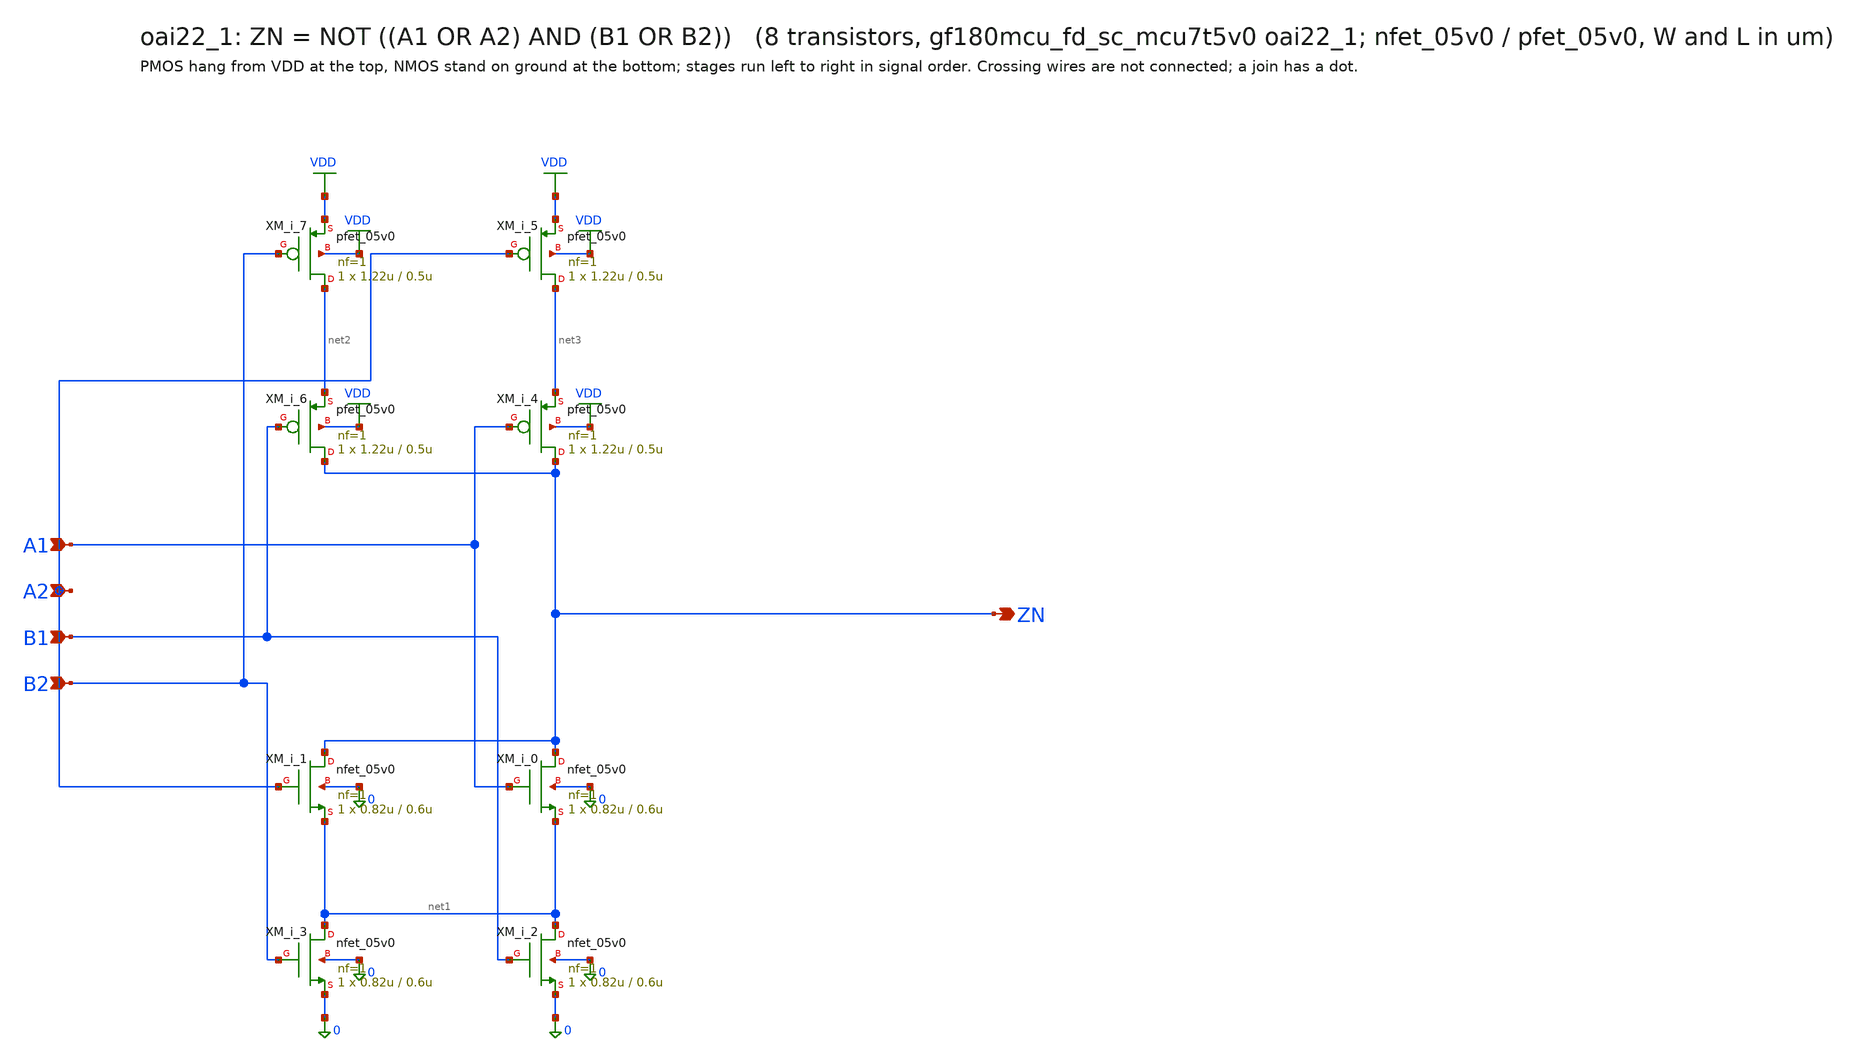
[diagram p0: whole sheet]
** sch_path: xschem/cells_tx/oai22_1.sch
**.subckt oai22_1 A1 A2 B1 B2 ZN
*.ipin A1
*.ipin A2
*.ipin B1
*.ipin B2
*.opin ZN
XM_i_3 net1 B2 0 0 nfet_05v0 L=0.6u W=0.82u nf=1 ad=4.1e-13 as=4.1e-13 pd=2.64e-06 ps=2.64e-06 nrd=0
+ nrs=0 sa=0 sb=0 sd=0 m=1
XM_i_2 net1 B1 0 0 nfet_05v0 L=0.6u W=0.82u nf=1 ad=4.1e-13 as=4.1e-13 pd=2.64e-06 ps=2.64e-06 nrd=0
+ nrs=0 sa=0 sb=0 sd=0 m=1
XM_i_0 ZN A1 net1 0 nfet_05v0 L=0.6u W=0.82u nf=1 ad=4.1e-13 as=4.1e-13 pd=2.64e-06 ps=2.64e-06
+ nrd=0 nrs=0 sa=0 sb=0 sd=0 m=1
XM_i_1 ZN A2 net1 0 nfet_05v0 L=0.6u W=0.82u nf=1 ad=4.1e-13 as=4.1e-13 pd=2.64e-06 ps=2.64e-06
+ nrd=0 nrs=0 sa=0 sb=0 sd=0 m=1
XM_i_7 net2 B2 VDD VDD pfet_05v0 L=0.5u W=1.22u nf=1 ad=6.1e-13 as=6.1e-13 pd=3.44e-06 ps=3.44e-06
+ nrd=0 nrs=0 sa=0 sb=0 sd=0 m=1
XM_i_6 ZN B1 net2 VDD pfet_05v0 L=0.5u W=1.22u nf=1 ad=6.1e-13 as=6.1e-13 pd=3.44e-06 ps=3.44e-06
+ nrd=0 nrs=0 sa=0 sb=0 sd=0 m=1
XM_i_4 ZN A1 net3 VDD pfet_05v0 L=0.5u W=1.22u nf=1 ad=6.1e-13 as=6.1e-13 pd=3.44e-06 ps=3.44e-06
+ nrd=0 nrs=0 sa=0 sb=0 sd=0 m=1
XM_i_5 net3 A2 VDD VDD pfet_05v0 L=0.5u W=1.22u nf=1 ad=6.1e-13 as=6.1e-13 pd=3.44e-06 ps=3.44e-06
+ nrd=0 nrs=0 sa=0 sb=0 sd=0 m=1
**.ends
.GLOBAL VDD
.end
